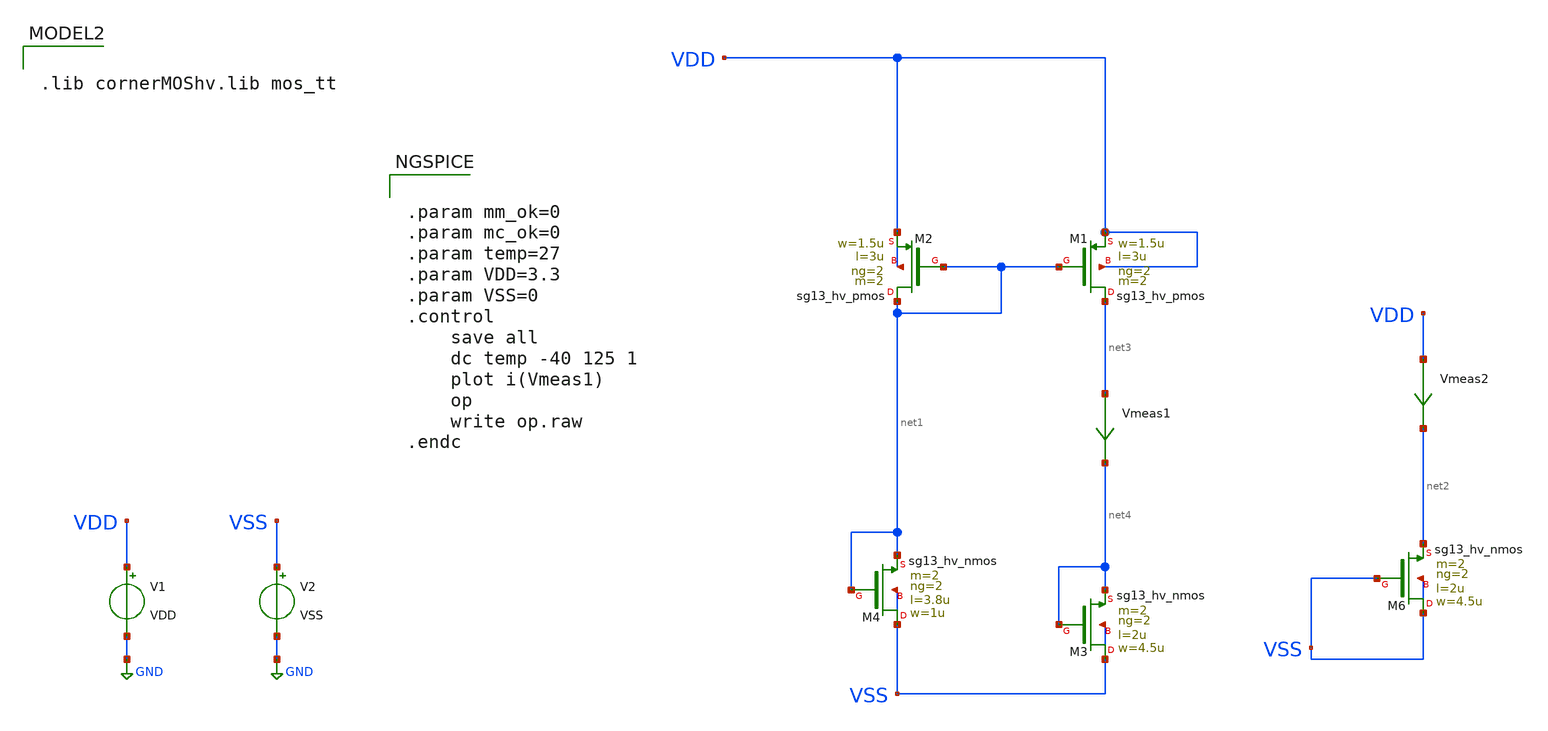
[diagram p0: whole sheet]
** sch_path: Learning/fully_differencial/Indirect_Compensation_Techniques_for_Three_Stage_Fully_Differential_Op_amps_IHP130/testbenches/transimpedance_cell_tb_.sch
**.subckt transimpedance_cell_tb_
V1 VDD GND VDD
V2 VSS GND VSS
XM1 net3 net1 VDD VDD sg13_hv_pmos w=1.5u l=3u ng=2 m=2 mm_ok=1
XM2 net1 net1 VDD VDD sg13_hv_pmos w=1.5u l=3u ng=2 m=2 mm_ok=1
XM6 VSS VSS net2 VSS sg13_hv_nmos w=4.5u l=2u ng=2 m=2 mm_ok=1
Vmeas2 VDD net2 0
.save i(vmeas2)
Vmeas1 net3 net4 0
.save i(vmeas1)
XM3 VSS net4 net4 VSS sg13_hv_nmos w=4.5u l=2u ng=2 m=2 mm_ok=1
XM4 VSS net1 net1 VSS sg13_hv_nmos w=1u l=3.8u ng=2 m=2 mm_ok=1
**** begin user architecture code


.param mm_ok=0
.param mc_ok=0
.param temp=27
.param VDD=3.3
.param VSS=0
.control
	save all
	dc temp -40 125 1
	plot i(Vmeas1)
	op
	write op.raw
.endc



.lib $::SG13G2_MODELS/cornerRES.lib res_typ


.lib cornerMOShv.lib mos_tt

**** end user architecture code
**.ends
.GLOBAL GND
.end
